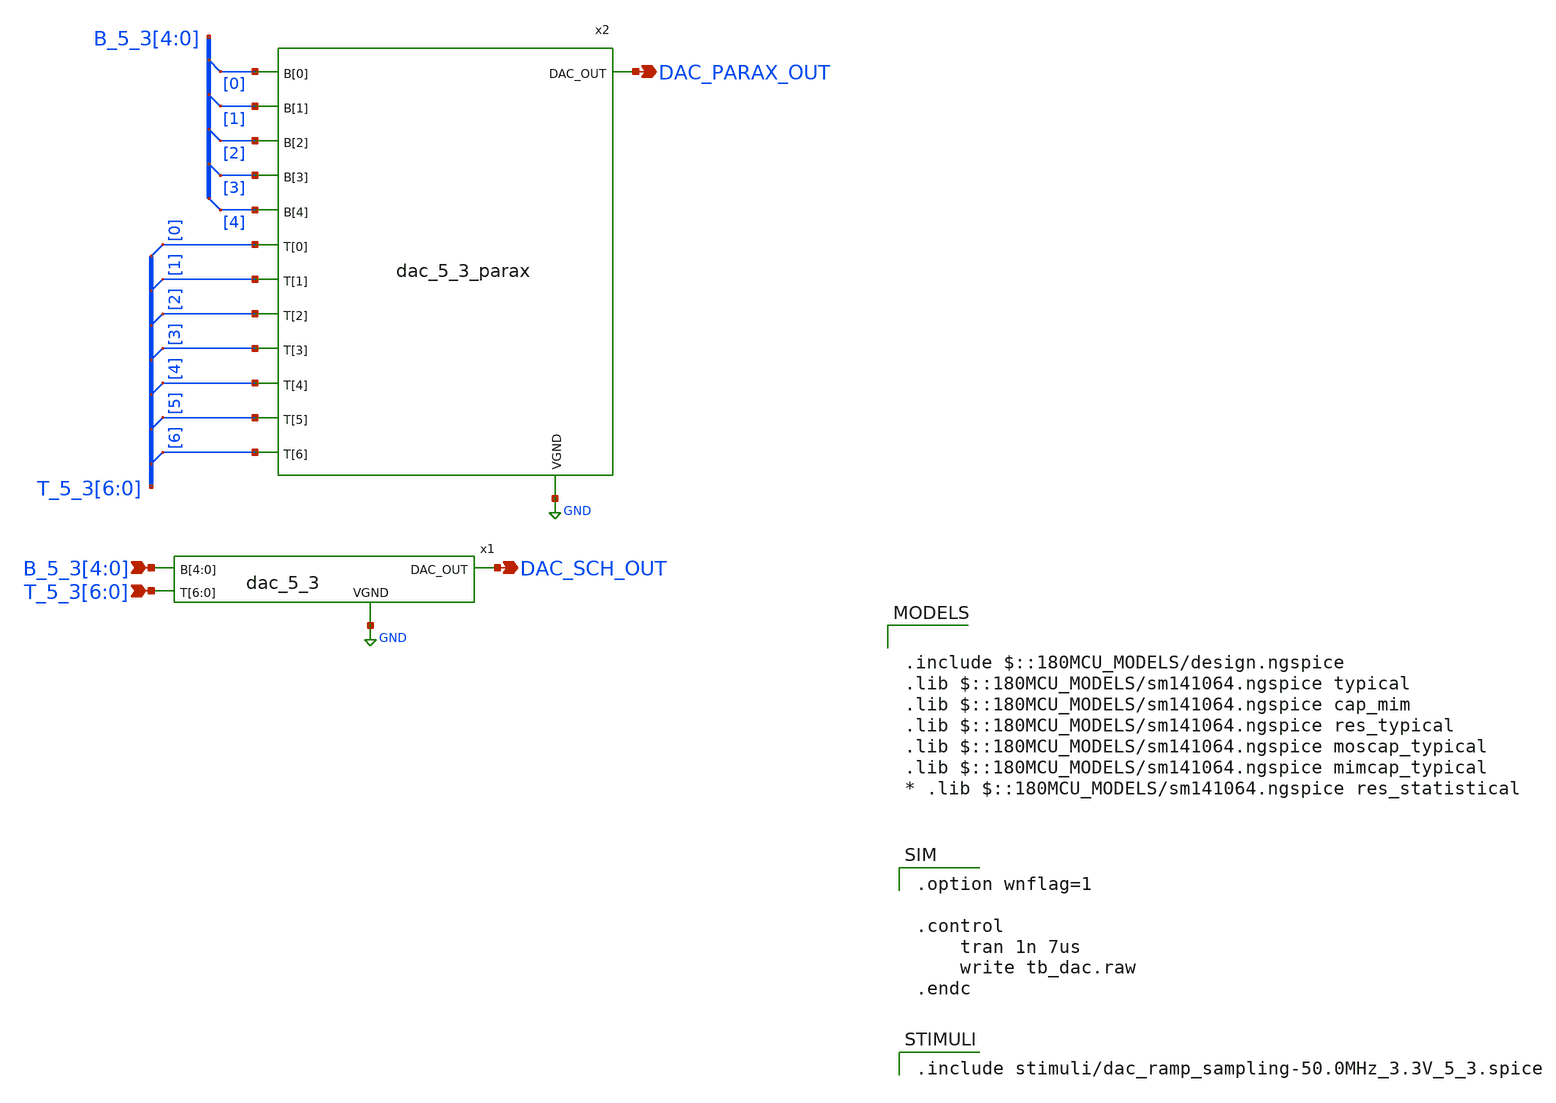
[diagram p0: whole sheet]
** sch_path: xschem/tb_dac.sch
**.subckt tb_dac DAC_PARAX_OUT B_5_3[4],B_5_3[3],B_5_3[2],B_5_3[1],B_5_3[0]
*+ T_5_3[6],T_5_3[5],T_5_3[4],T_5_3[3],T_5_3[2],T_5_3[1],T_5_3[0] DAC_SCH_OUT
*.opin DAC_PARAX_OUT
*.ipin B_5_3[4],B_5_3[3],B_5_3[2],B_5_3[1],B_5_3[0]
*.ipin T_5_3[6],T_5_3[5],T_5_3[4],T_5_3[3],T_5_3[2],T_5_3[1],T_5_3[0]
*.opin DAC_SCH_OUT
x2 B_5_3[0] B_5_3[1] B_5_3[2] B_5_3[3] B_5_3[4] T_5_3[0] T_5_3[1] T_5_3[2] T_5_3[3] T_5_3[4]
+ T_5_3[5] T_5_3[6] DAC_PARAX_OUT GND dac_5_3_parax
* tap: B_5_3[4:0] --> B_5_3[0]
* tap: B_5_3[4:0] --> B_5_3[1]
* tap: B_5_3[4:0] --> B_5_3[2]
* tap: B_5_3[4:0] --> B_5_3[3]
* tap: B_5_3[4:0] --> B_5_3[4]
* tap: T_5_3[6:0] --> T_5_3[0]
* tap: T_5_3[6:0] --> T_5_3[1]
* tap: T_5_3[6:0] --> T_5_3[2]
* tap: T_5_3[6:0] --> T_5_3[3]
* tap: T_5_3[6:0] --> T_5_3[4]
* tap: T_5_3[6:0] --> T_5_3[5]
* tap: T_5_3[6:0] --> T_5_3[6]
x1 DAC_SCH_OUT B_5_3[4] B_5_3[3] B_5_3[2] B_5_3[1] B_5_3[0] T_5_3[6] T_5_3[5] T_5_3[4] T_5_3[3]
+ T_5_3[2] T_5_3[1] T_5_3[0] GND dac_5_3
**** begin user architecture code

.option wnflag=1

.control
    tran 1n 7us
    write tb_dac.raw
.endc



.include stimuli/dac_ramp_sampling-50.0MHz_3.3V_5_3.spice


.include $::180MCU_MODELS/design.ngspice
.lib $::180MCU_MODELS/sm141064.ngspice typical
.lib $::180MCU_MODELS/sm141064.ngspice cap_mim
.lib $::180MCU_MODELS/sm141064.ngspice res_typical
.lib $::180MCU_MODELS/sm141064.ngspice moscap_typical
.lib $::180MCU_MODELS/sm141064.ngspice mimcap_typical
* .lib $::180MCU_MODELS/sm141064.ngspice res_statistical

**** end user architecture code
**.ends
.GLOBAL GND
.end
